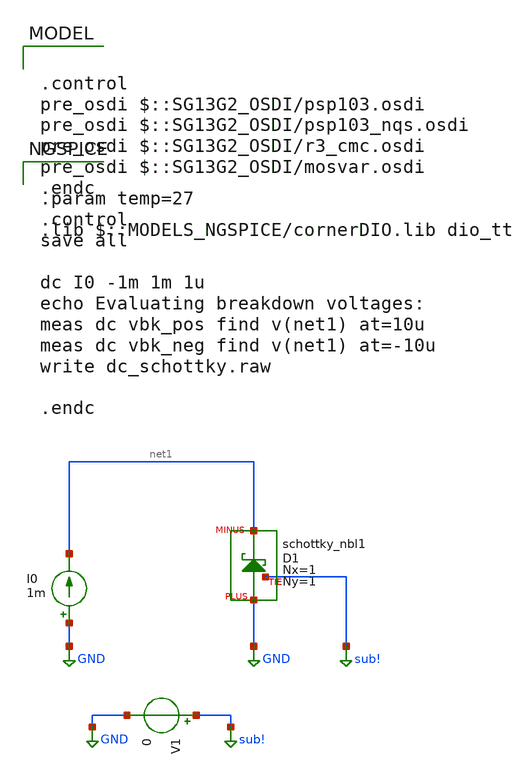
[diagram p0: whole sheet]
** sch_path: ihp-sg13g2/xschem_libs/sg13g2_tests/dc_schottky/schematic/dc_schottky.sch
* Copyright 2023 IHP PDK Authors
**.subckt dc_schottky
I0 GND net1 1m
XD1 GND net1 sub! schottky_nbl1 Nx=1 Ny=1
V1 sub! GND 0
**** begin user architecture code

.control
pre_osdi $::SG13G2_OSDI/psp103.osdi
pre_osdi $::SG13G2_OSDI/psp103_nqs.osdi
pre_osdi $::SG13G2_OSDI/r3_cmc.osdi
pre_osdi $::SG13G2_OSDI/mosvar.osdi
.endc

.lib $::MODELS_NGSPICE/cornerDIO.lib dio_tt



.param temp=27
.control
save all

dc I0 -1m 1m 1u
echo Evaluating breakdown voltages:
meas dc vbk_pos find v(net1) at=10u
meas dc vbk_neg find v(net1) at=-10u
write dc_schottky.raw

.endc


**** end user architecture code
**.ends
.GLOBAL GND
.GLOBAL sub!
.end
